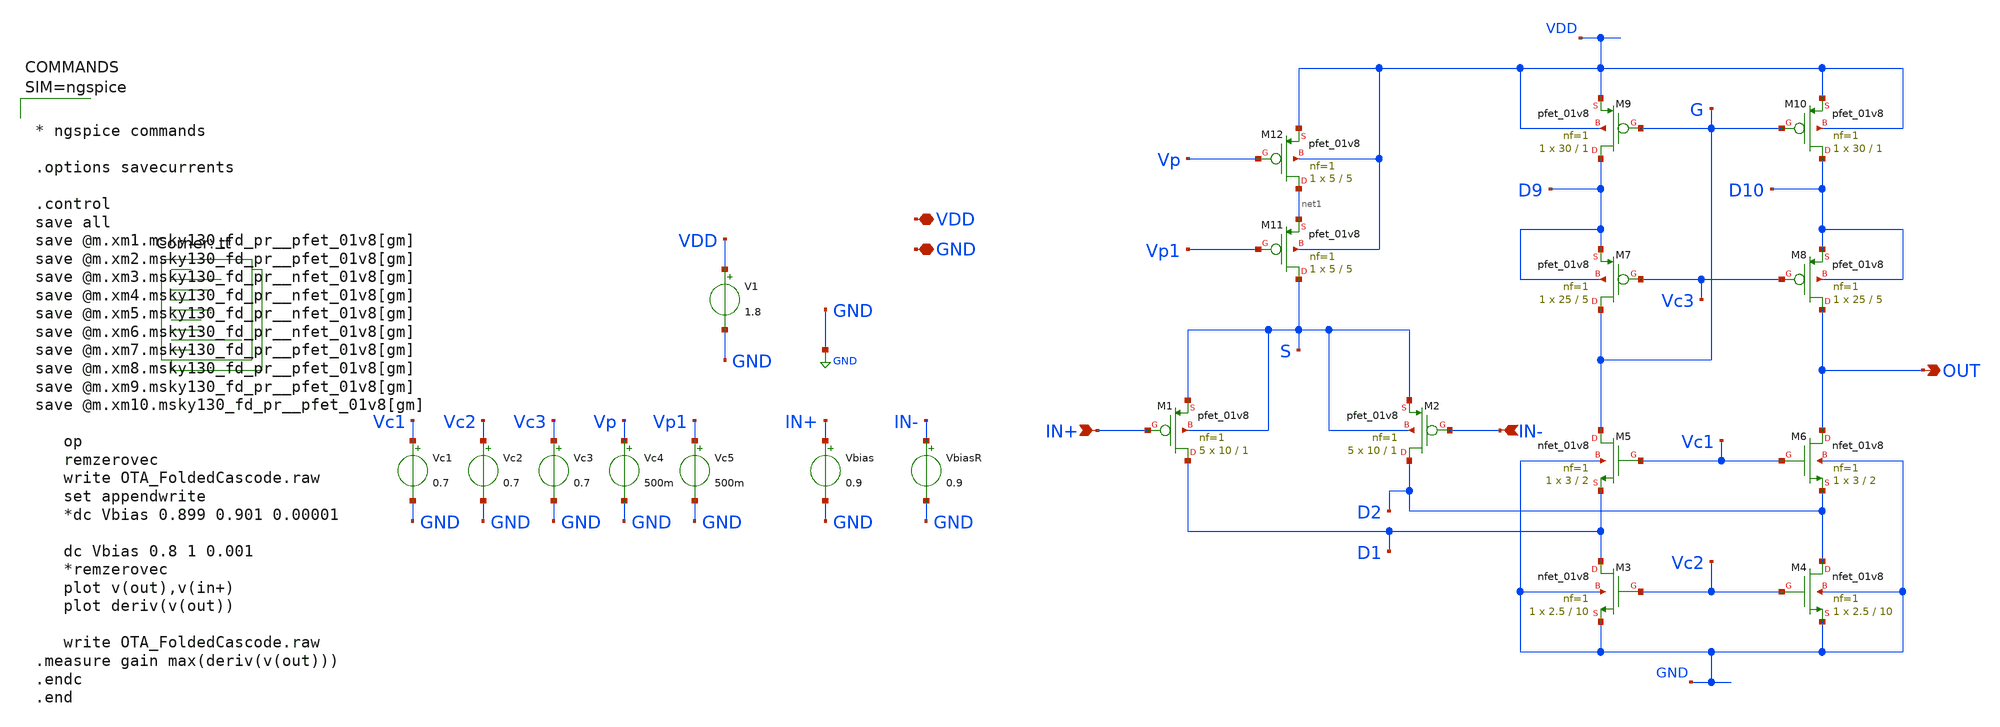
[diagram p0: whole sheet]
** sch_path: xschem/OTA_FoldedCascode.sch
**.subckt OTA_FoldedCascode VDD GND IN+ IN- OUT
*.iopin VDD
*.iopin GND
*.ipin IN+
*.ipin IN-
*.opin OUT
V1 VDD GND 1.8
Vbias IN+ GND 0.9
VbiasR IN- GND 0.9
XM1 D1 IN+ S S sky130_fd_pr__pfet_01v8 L=1 W=10 nf=1 ad='int((nf+1)/2) * W/nf * 0.29' as='int((nf+2)/2) * W/nf * 0.29'
+ pd='2*int((nf+1)/2) * (W/nf + 0.29)' ps='2*int((nf+2)/2) * (W/nf + 0.29)' nrd='0.29 / W' nrs='0.29 / W'
+ sa=0 sb=0 sd=0 mult=5 m=5
XM2 D2 IN- S S sky130_fd_pr__pfet_01v8 L=1 W=10 nf=1 ad='int((nf+1)/2) * W/nf * 0.29' as='int((nf+2)/2) * W/nf * 0.29'
+ pd='2*int((nf+1)/2) * (W/nf + 0.29)' ps='2*int((nf+2)/2) * (W/nf + 0.29)' nrd='0.29 / W' nrs='0.29 / W'
+ sa=0 sb=0 sd=0 mult=5 m=5
XM3 D1 Vc2 GND GND sky130_fd_pr__nfet_01v8 L=10 W=2.5 nf=1 ad='int((nf+1)/2) * W/nf * 0.29' as='int((nf+2)/2) * W/nf * 0.29'
+ pd='2*int((nf+1)/2) * (W/nf + 0.29)' ps='2*int((nf+2)/2) * (W/nf + 0.29)' nrd='0.29 / W' nrs='0.29 / W'
+ sa=0 sb=0 sd=0 mult=1 m=1
XM4 D2 Vc2 GND GND sky130_fd_pr__nfet_01v8 L=10 W=2.5 nf=1 ad='int((nf+1)/2) * W/nf * 0.29' as='int((nf+2)/2) * W/nf * 0.29'
+ pd='2*int((nf+1)/2) * (W/nf + 0.29)' ps='2*int((nf+2)/2) * (W/nf + 0.29)' nrd='0.29 / W' nrs='0.29 / W'
+ sa=0 sb=0 sd=0 mult=1 m=1
XM5 G Vc1 D1 GND sky130_fd_pr__nfet_01v8 L=2 W=3 nf=1 ad='int((nf+1)/2) * W/nf * 0.29' as='int((nf+2)/2) * W/nf * 0.29'
+ pd='2*int((nf+1)/2) * (W/nf + 0.29)' ps='2*int((nf+2)/2) * (W/nf + 0.29)' nrd='0.29 / W' nrs='0.29 / W'
+ sa=0 sb=0 sd=0 mult=1 m=1
XM6 OUT Vc1 D2 GND sky130_fd_pr__nfet_01v8 L=2 W=3 nf=1 ad='int((nf+1)/2) * W/nf * 0.29' as='int((nf+2)/2) * W/nf * 0.29'
+ pd='2*int((nf+1)/2) * (W/nf + 0.29)' ps='2*int((nf+2)/2) * (W/nf + 0.29)' nrd='0.29 / W' nrs='0.29 / W'
+ sa=0 sb=0 sd=0 mult=1 m=1
XM7 G Vc3 D9 D9 sky130_fd_pr__pfet_01v8 L=5 W=25 nf=1 ad='int((nf+1)/2) * W/nf * 0.29' as='int((nf+2)/2) * W/nf * 0.29'
+ pd='2*int((nf+1)/2) * (W/nf + 0.29)' ps='2*int((nf+2)/2) * (W/nf + 0.29)' nrd='0.29 / W' nrs='0.29 / W'
+ sa=0 sb=0 sd=0 mult=1 m=1
XM8 OUT Vc3 D10 D10 sky130_fd_pr__pfet_01v8 L=5 W=25 nf=1 ad='int((nf+1)/2) * W/nf * 0.29' as='int((nf+2)/2) * W/nf * 0.29'
+ pd='2*int((nf+1)/2) * (W/nf + 0.29)' ps='2*int((nf+2)/2) * (W/nf + 0.29)' nrd='0.29 / W' nrs='0.29 / W'
+ sa=0 sb=0 sd=0 mult=1 m=1
XM9 D9 G VDD VDD sky130_fd_pr__pfet_01v8 L=1 W=30 nf=1 ad='int((nf+1)/2) * W/nf * 0.29' as='int((nf+2)/2) * W/nf * 0.29'
+ pd='2*int((nf+1)/2) * (W/nf + 0.29)' ps='2*int((nf+2)/2) * (W/nf + 0.29)' nrd='0.29 / W' nrs='0.29 / W'
+ sa=0 sb=0 sd=0 mult=1 m=1
XM10 D10 G VDD VDD sky130_fd_pr__pfet_01v8 L=1 W=30 nf=1 ad='int((nf+1)/2) * W/nf * 0.29' as='int((nf+2)/2) * W/nf * 0.29'
+ pd='2*int((nf+1)/2) * (W/nf + 0.29)' ps='2*int((nf+2)/2) * (W/nf + 0.29)' nrd='0.29 / W' nrs='0.29 / W'
+ sa=0 sb=0 sd=0 mult=1 m=1
Vc1 Vc1 GND 0.7
Vc2 Vc2 GND 0.7
Vc3 Vc3 GND 0.7
Vc4 Vp GND 500m
XM11 S Vp1 net1 VDD sky130_fd_pr__pfet_01v8 L=5 W=5 nf=1 ad='int((nf+1)/2) * W/nf * 0.29' as='int((nf+2)/2) * W/nf * 0.29'
+ pd='2*int((nf+1)/2) * (W/nf + 0.29)' ps='2*int((nf+2)/2) * (W/nf + 0.29)' nrd='0.29 / W' nrs='0.29 / W'
+ sa=0 sb=0 sd=0 mult=1 m=1
XM12 net1 Vp VDD VDD sky130_fd_pr__pfet_01v8 L=5 W=5 nf=1 ad='int((nf+1)/2) * W/nf * 0.29' as='int((nf+2)/2) * W/nf * 0.29'
+ pd='2*int((nf+1)/2) * (W/nf + 0.29)' ps='2*int((nf+2)/2) * (W/nf + 0.29)' nrd='0.29 / W' nrs='0.29 / W'
+ sa=0 sb=0 sd=0 mult=1 m=1
Vc5 Vp1 GND 500m
**** begin user architecture code



* ngspice commands

.options savecurrents

.control
save all
save @m.xm1.msky130_fd_pr__pfet_01v8[gm]
save @m.xm2.msky130_fd_pr__pfet_01v8[gm]
save @m.xm3.msky130_fd_pr__nfet_01v8[gm]
save @m.xm4.msky130_fd_pr__nfet_01v8[gm]
save @m.xm5.msky130_fd_pr__nfet_01v8[gm]
save @m.xm6.msky130_fd_pr__nfet_01v8[gm]
save @m.xm7.msky130_fd_pr__pfet_01v8[gm]
save @m.xm8.msky130_fd_pr__pfet_01v8[gm]
save @m.xm9.msky130_fd_pr__pfet_01v8[gm]
save @m.xm10.msky130_fd_pr__pfet_01v8[gm]

   op
   remzerovec
   write OTA_FoldedCascode.raw
   set appendwrite
   *dc Vbias 0.899 0.901 0.00001

   dc Vbias 0.8 1 0.001
   *remzerovec
   plot v(out),v(in+)
   plot deriv(v(out))

   write OTA_FoldedCascode.raw
.measure gain max(deriv(v(out)))
.endc
.end



.lib $::SKYWATER_MODELS/sky130.lib.spice tt
**** end user architecture code
**.ends
.GLOBAL GND
.end
